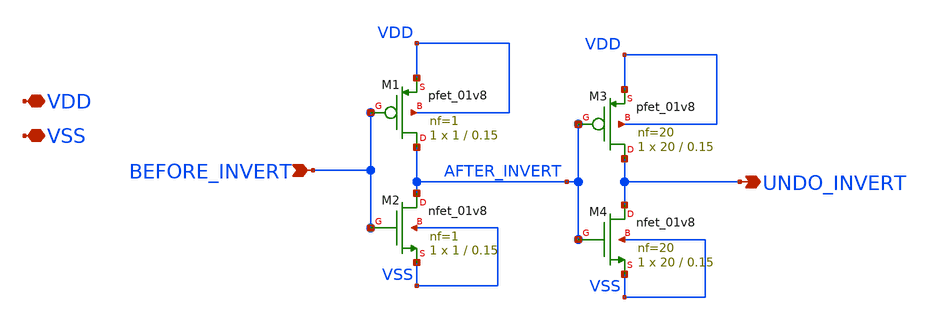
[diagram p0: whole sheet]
** sch_path: xschem/double_inverter.sch
**.subckt double_inverter VDD VSS BEFORE_INVERT UNDO_INVERT
*.iopin VDD
*.iopin VSS
*.ipin BEFORE_INVERT
*.opin UNDO_INVERT
XM1 AFTER_INVERT BEFORE_INVERT VDD VDD sky130_fd_pr__pfet_01v8 L=0.15 W=1 nf=1 ad='int((nf+1)/2) * W/nf * 0.29'
+ as='int((nf+2)/2) * W/nf * 0.29' pd='2*int((nf+1)/2) * (W/nf + 0.29)' ps='2*int((nf+2)/2) * (W/nf + 0.29)'
+ nrd='0.29 / W' nrs='0.29 / W' sa=0 sb=0 sd=0 mult=1 m=1
XM2 AFTER_INVERT BEFORE_INVERT VSS VSS sky130_fd_pr__nfet_01v8 L=0.15 W=1 nf=1 ad='int((nf+1)/2) * W/nf * 0.29'
+ as='int((nf+2)/2) * W/nf * 0.29' pd='2*int((nf+1)/2) * (W/nf + 0.29)' ps='2*int((nf+2)/2) * (W/nf + 0.29)'
+ nrd='0.29 / W' nrs='0.29 / W' sa=0 sb=0 sd=0 mult=1 m=1
XM3 UNDO_INVERT AFTER_INVERT VDD VDD sky130_fd_pr__pfet_01v8 L=0.15 W=20 nf=20 ad='int((nf+1)/2) * W/nf * 0.29'
+ as='int((nf+2)/2) * W/nf * 0.29' pd='2*int((nf+1)/2) * (W/nf + 0.29)' ps='2*int((nf+2)/2) * (W/nf + 0.29)'
+ nrd='0.29 / W' nrs='0.29 / W' sa=0 sb=0 sd=0 mult=1 m=1
XM4 UNDO_INVERT AFTER_INVERT VSS VSS sky130_fd_pr__nfet_01v8 L=0.15 W=20 nf=20 ad='int((nf+1)/2) * W/nf * 0.29'
+ as='int((nf+2)/2) * W/nf * 0.29' pd='2*int((nf+1)/2) * (W/nf + 0.29)' ps='2*int((nf+2)/2) * (W/nf + 0.29)'
+ nrd='0.29 / W' nrs='0.29 / W' sa=0 sb=0 sd=0 mult=1 m=1
**.ends
.end
